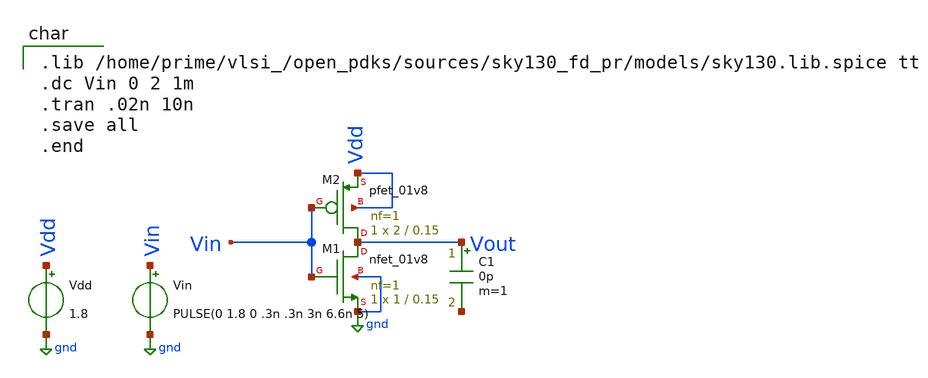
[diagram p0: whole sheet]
** sch_path: schematics/inverter_simulation.sch
**.subckt inverter_simulation
Vdd Vdd gnd 1.8
Vin Vin gnd PULSE(0 1.8 0 .3n .3n 3n 6.6n 5)
C1 Vout net1 0p m=1
XM1 Vout Vin gnd gnd sky130_fd_pr__nfet_01v8 L=0.15 W=1 nf=1 ad='int((1 + 1)/2) * 1 / 1 * 0.29' as='int((1 + 2)/2) * 1 / 1 * 0.29'
+ pd='2*int((1 + 1)/2) * (1 / 1 + 0.29)' ps='2*int((1 + 2)/2) * (1 / 1 + 0.29)' nrd='0.29 / 1 ' nrs='0.29 / 1 '
+ sa=0 sb=0 sd=0 mult=1 m=1
XM2 Vout Vin Vdd Vdd sky130_fd_pr__pfet_01v8 L=0.15 W=2 nf=1 ad='int((1 + 1)/2) * 2 / 1 * 0.29' as='int((1 + 2)/2) * 2 / 1 * 0.29'
+ pd='2*int((1 + 1)/2) * (2 / 1 + 0.29)' ps='2*int((1 + 2)/2) * (2 / 1 + 0.29)' nrd='0.29 / 2 ' nrs='0.29 / 2 '
+ sa=0 sb=0 sd=0 mult=1 m=1
**** begin user architecture code

.lib /home/prime/vlsi_/open_pdks/sources/sky130_fd_pr/models/sky130.lib.spice tt
.dc Vin 0 2 1m
.tran .02n 10n
.save all
.end

**** end user architecture code
**.ends
.GLOBAL gnd
.end
